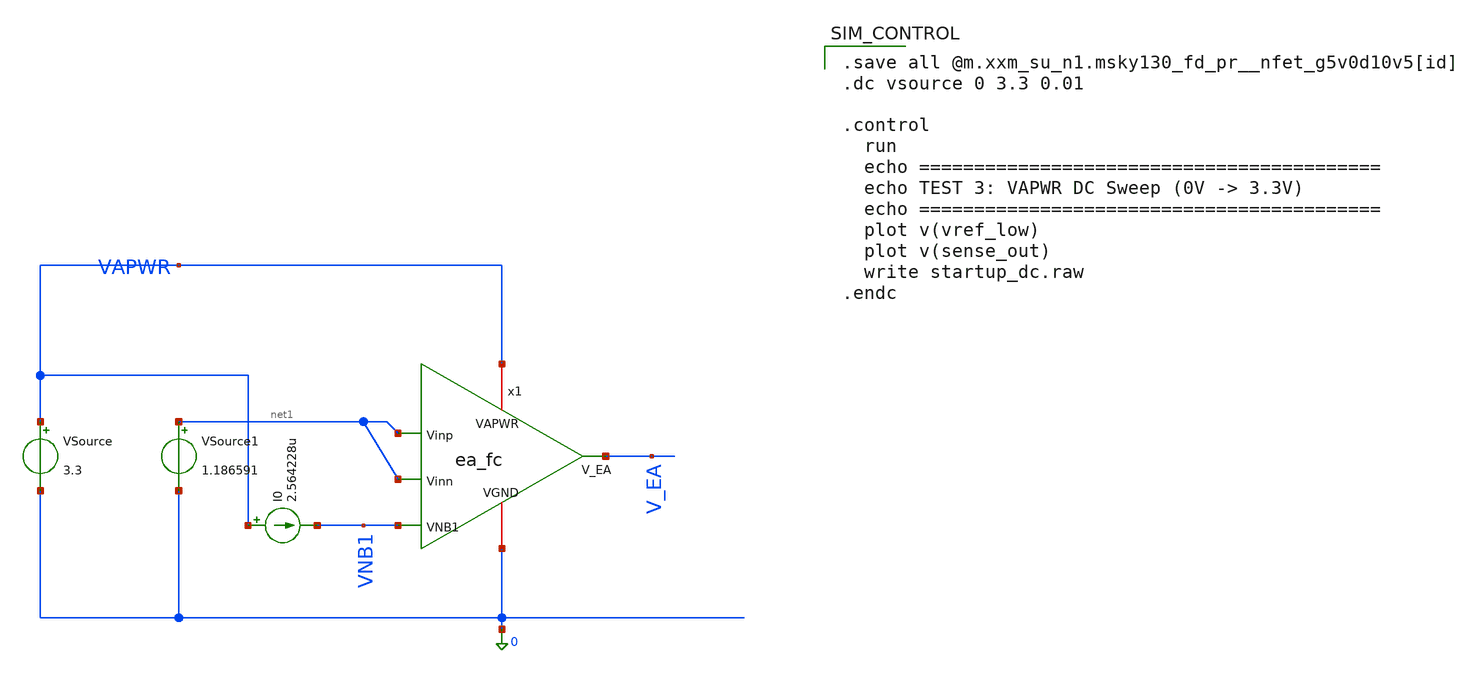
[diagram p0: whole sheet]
** sch_path: designs/bgr_ldo/ldo/ea_fc_tb.sch
**.subckt ea_fc_tb
x1 VAPWR V_EA net1 net1 VNB1 0 ea_fc
VSource VAPWR 0 3.3
I0 VAPWR VNB1 2.564228u
VSource1 net1 0 1.186591
**** begin user architecture code

** opencircuitdesign pdks install
.lib $::SKYWATER_MODELS/sky130.lib.spice tt


.save all @m.xxm_su_n1.msky130_fd_pr__nfet_g5v0d10v5[id]
.dc vsource 0 3.3 0.01

.control
  run
  echo ==========================================
  echo TEST 3: VAPWR DC Sweep (0V -> 3.3V)
  echo ==========================================
  plot v(vref_low)
  plot v(sense_out)
  write startup_dc.raw
.endc

**** end user architecture code
**.ends
.end
